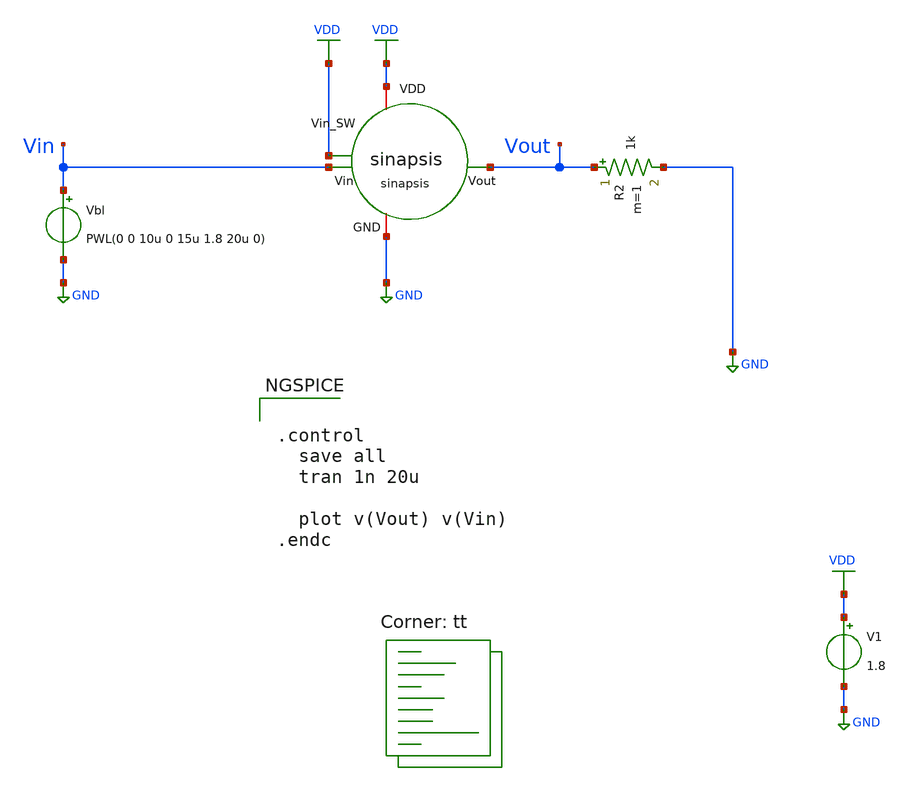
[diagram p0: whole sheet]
** sch_path: hopfield/sinapsis_y_nerona.sch
**.subckt sinapsis_y_nerona
x1 VDD VDD Vout Vin GND sinapsis
V1 VDD GND 1.8
Vbl Vin GND PWL(0 0 10u 0 15u 1.8 20u 0)
R2 Vout GND 1k m=1
**** begin user architecture code


.control
  save all
  tran 1n 20u

  plot v(Vout) v(Vin)
.endc



.lib $::SKYWATER_MODELS/sky130.lib.spice tt

** opencircuitdesign pdks install
.inc $::SKYWATER_MODELS/rram_v0.spice

**** end user architecture code
**.ends
.GLOBAL VDD
.GLOBAL GND
.end
